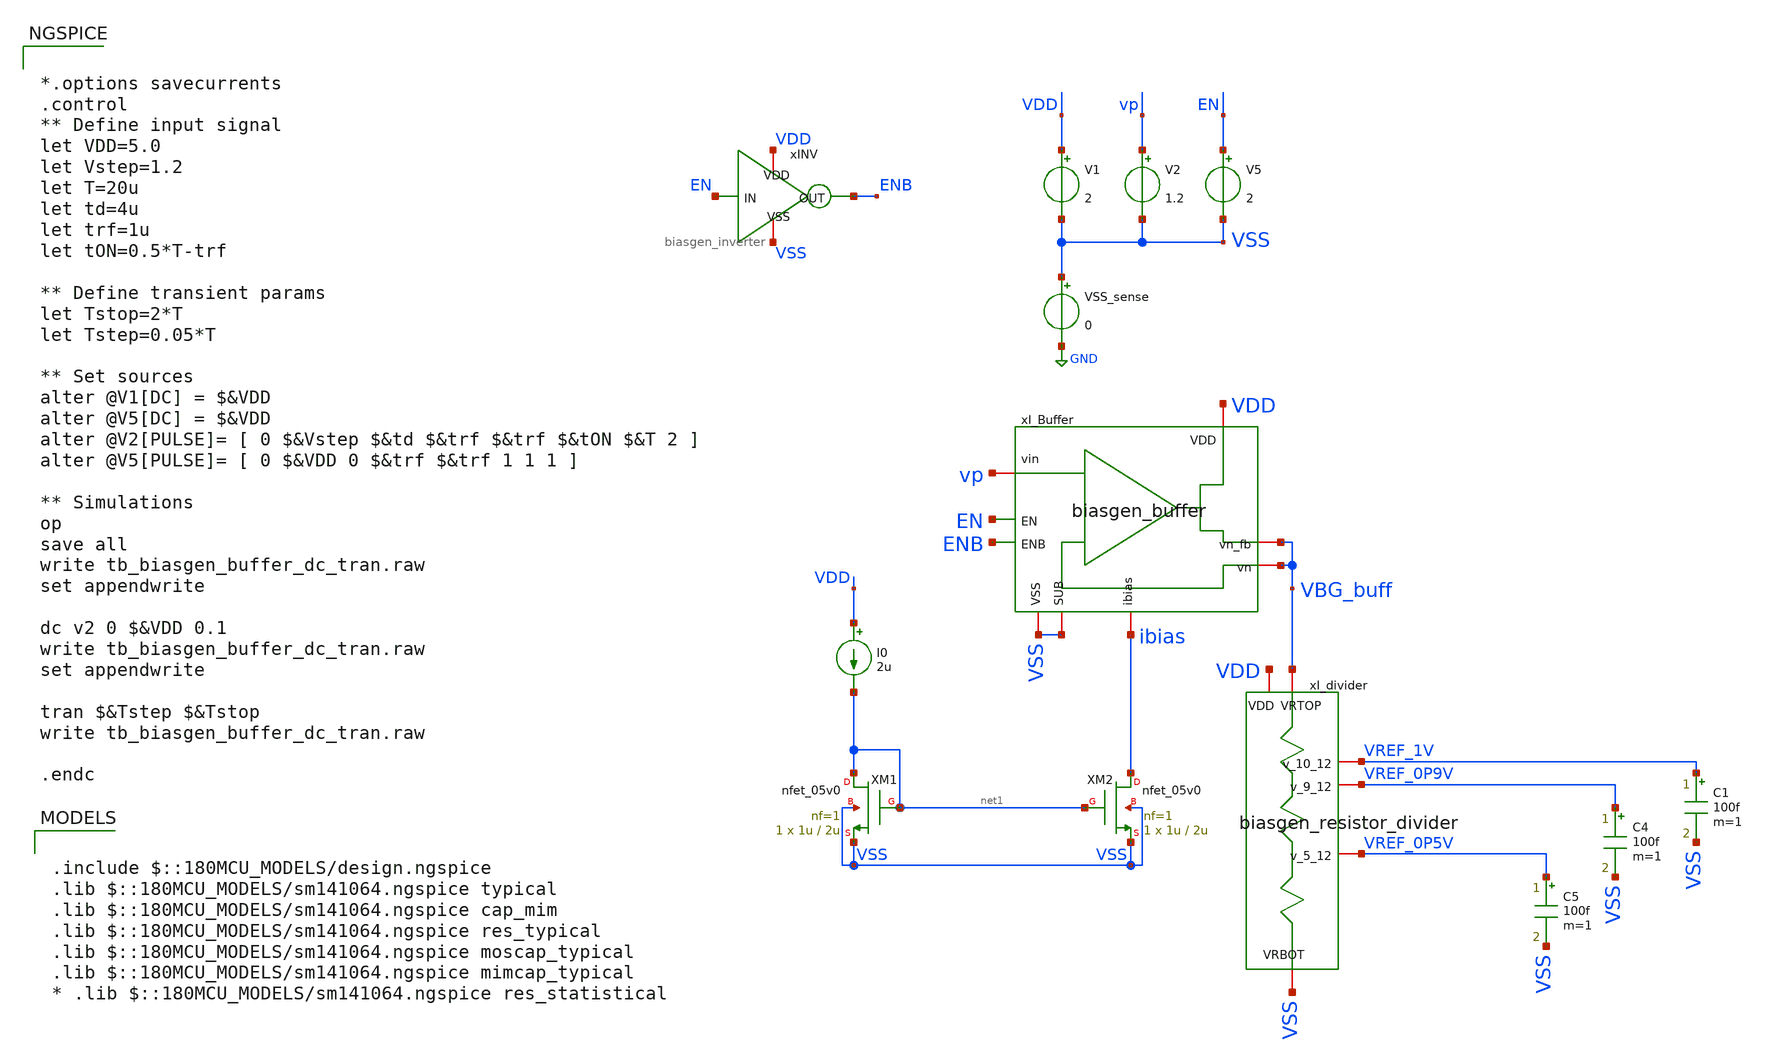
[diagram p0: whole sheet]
** sch_path: designs/libs/tb_biasgen/tb_biasgen_buffer_dc_tran/tb_biasgen_buffer_dc_tran.sch
**.subckt tb_biasgen_buffer_dc_tran
V1 VDD VSS 2
V2 vp VSS 1.2
VSS_sense VSS GND 0
I0 VDD net1 2u
xI_Buffer VDD EN ENB vp VSS ibias VBG_buff VBG_buff VSS biasgen_buffer
xI_divider VBG_buff VDD VREF_1V VREF_0P9V VREF_0P5V VSS biasgen_resistor_divider
C1 VREF_1V VSS 100f m=1
C4 VREF_0P9V VSS 100f m=1
C5 VREF_0P5V VSS 100f m=1
xINV VDD EN ENB VSS biasgen_inverter
V5 EN VSS 2
XM1 net1 net1 VSS VSS nfet_05v0 L=2u W=1u nf=1 ad='int((nf+1)/2) * W/nf * 0.18u' as='int((nf+2)/2) * W/nf * 0.18u'
+ pd='2*int((nf+1)/2) * (W/nf + 0.18u)' ps='2*int((nf+2)/2) * (W/nf + 0.18u)' nrd='0.18u / W' nrs='0.18u / W'
+ sa=0 sb=0 sd=0 m=1
XM2 ibias net1 VSS VSS nfet_05v0 L=2u W=1u nf=1 ad='int((nf+1)/2) * W/nf * 0.18u' as='int((nf+2)/2) * W/nf * 0.18u'
+ pd='2*int((nf+1)/2) * (W/nf + 0.18u)' ps='2*int((nf+2)/2) * (W/nf + 0.18u)' nrd='0.18u / W' nrs='0.18u / W'
+ sa=0 sb=0 sd=0 m=1
**** begin user architecture code

.include $::180MCU_MODELS/design.ngspice
.lib $::180MCU_MODELS/sm141064.ngspice typical
.lib $::180MCU_MODELS/sm141064.ngspice cap_mim
.lib $::180MCU_MODELS/sm141064.ngspice res_typical
.lib $::180MCU_MODELS/sm141064.ngspice moscap_typical
.lib $::180MCU_MODELS/sm141064.ngspice mimcap_typical
* .lib $::180MCU_MODELS/sm141064.ngspice res_statistical



*.options savecurrents
.control
** Define input signal
let VDD=5.0
let Vstep=1.2
let T=20u
let td=4u
let trf=1u
let tON=0.5*T-trf

** Define transient params
let Tstop=2*T
let Tstep=0.05*T

** Set sources
alter @V1[DC] = $&VDD
alter @V5[DC] = $&VDD
alter @V2[PULSE]= [ 0 $&Vstep $&td $&trf $&trf $&tON $&T 2 ]
alter @V5[PULSE]= [ 0 $&VDD 0 $&trf $&trf 1 1 1 ]

** Simulations
op
save all
write tb_biasgen_buffer_dc_tran.raw
set appendwrite

dc v2 0 $&VDD 0.1
write tb_biasgen_buffer_dc_tran.raw
set appendwrite

tran $&Tstep $&Tstop
write tb_biasgen_buffer_dc_tran.raw

.endc


**** end user architecture code
**.ends
.GLOBAL GND
.end
